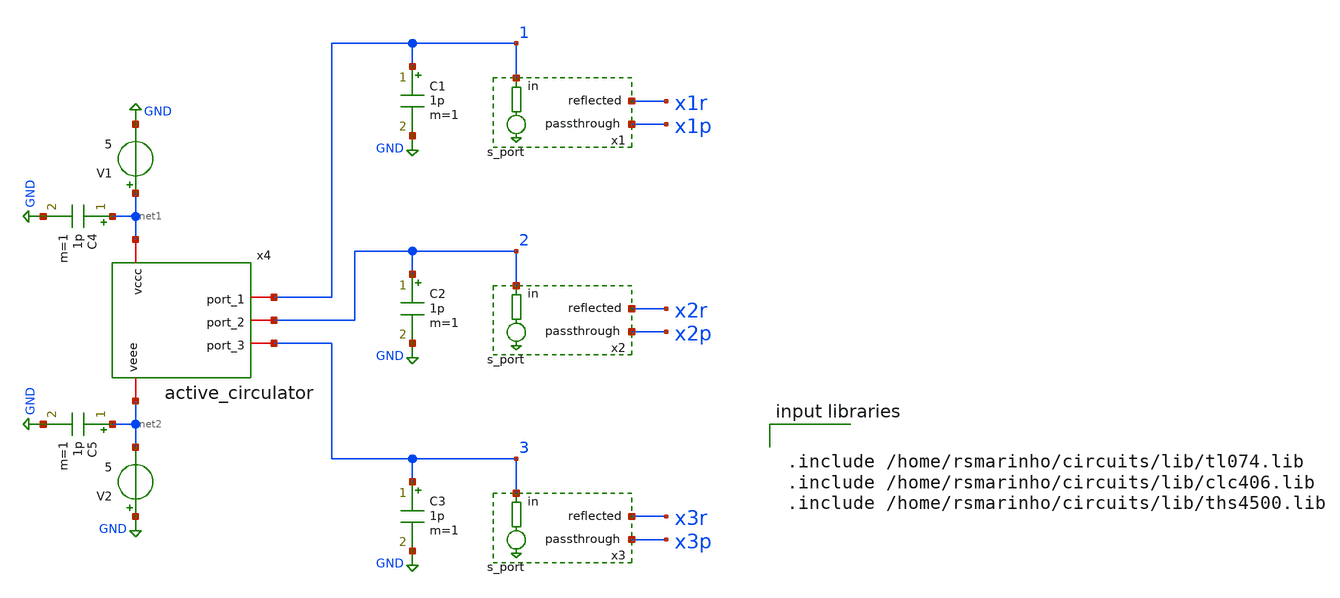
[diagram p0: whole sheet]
** sch_path: circulator/circulator_sparam.sch
**.subckt circulator_sparam
V1 net1 GND 5
V2 GND net2 5
C1 1 GND 1p m=1
C2 2 GND 1p m=1
C3 3 GND 1p m=1
C4 net1 GND 1p m=1
C5 net2 GND 1p m=1
x1 1 x1p x1r s_port Rbase=50 RS1=1e-6 RS2=1e12
x2 2 x2p x2r s_port Rbase=50 RS1=1e-6 RS2=1e12
x3 3 x3p x3r s_port Rbase=50 RS1=1e-6 RS2=1e12
x4 1 net1 2 3 net2 active_circulator
**** begin user architecture code



.options method=gear
.options savecurrents
.save all

** Check the two ac lines below for being equal!
.control
set noaskquit
set filetype=ascii

alter @c1[c] = 10p
alter @c2[c] = 10p
alter @c3[c] = 10p

** set input and output

alter R.x1.R1 = 1e-6
alter R.x1.R2 = 1e12

alter R.x2.R1 = 1e12
alter R.x2.R2 = 1e-6
alter R.x3.R1 = 1e12
alter R.x3.R2 = 1e-6

*** measurement for s11 and s21
op
** first ac measurement (change this line only together with following ac line)
ac lin 1000 1Meg 2G

**

** switch input and output

alter R.x2.R1 = 1e-6
alter R.x2.R2 = 1e12

alter R.x1.R1 = 1e12
alter R.x1.R2 = 1e-6
alter R.x3.R1 = 1e12
alter R.x3.R2 = 1e-6

*** measurement for s12 and s22
op
** second ac measurement (change this line only together with ac line above)
ac lin 1000 1Meg 2G

**

** switch input and output

alter R.x3.R1 = 1e-6
alter R.x3.R2 = 1e12

alter R.x1.R1 = 1e12
alter R.x1.R2 = 1e-6
alter R.x2.R1 = 1e12
alter R.x2.R2 = 1e-6

*** measurement for s12 and s22
op
** second ac measurement (change this line only together with ac line above)
ac lin 1000 1Meg 2G

**

** set s-param
let s11 = ac1.x1r
let s21 = ac1.x2p
let s31 = ac1.x3p

let s12 = ac2.x1p
let s22 = ac2.x2r
let s32 = ac2.x3p

let s13 = ac3.x1p
let s23 = ac3.x2p
let s33 = ac3.x3r

settype s-param s11 s21 s31 s12 s22 s32 s13 s23 s33


** set s-param db
let s11db = db(s11)
let s21db = db(s21)
let s31db = db(s31)

let s12db = db(s12)
let s22db = db(s22)
let s32db = db(s32)

let s13db = db(s13)
let s23db = db(s23)
let s33db = db(s33)

settype decibel s11db s21db s31db s12db s22db s32db s13db s23db s33db

** plot

plot xlog s11db s21db s31db
plot xlog s12db s22db s32db
plot xlog s13db s23db s33db

* gain
*plot xlog s12db s23db s31db

* isolation
*plot xlog s21db s32db s13db

* reflection
*plot xlog s11db s22db s33db

.endc
.end



.include /home/rsmarinho/circuits/lib/tl074.lib
.include /home/rsmarinho/circuits/lib/clc406.lib
.include /home/rsmarinho/circuits/lib/ths4500.lib

**** end user architecture code
**.ends

* expanding   symbol:  sparam/s_port.sym # of pins=3
** sym_path: sparam/s_port.sym
** sch_path: sparam/s_port.sch
.subckt s_port in passthrough reflected  Rbase=50 RS1=1e-6 RS2=1e12
*.iopin in
*.opin reflected
*.opin passthrough
Rout s2 8 Rbase m=1
Vdc 8 GND DC {Vbias_out} AC 0
E2 passthrough GND s2 GND 2
Vacdc 1 GND DC {Vbias_in} AC 1
Rin 1 s1 Rbase m=1
E1 3 GND s1 GND 2
Vac 3 4 DC 0 AC 1
Rloop reflected 4 1e-6 m=1
R3 reflected GND 1 m=1
.param Vbias_in = 0
R1 in s1 {RS1} m=1
R2 in s2 {RS2} m=1
.param Vbias_out = 0
.ends


* expanding   symbol:  circulator/active_circulator.sym # of pins=5
** sym_path: circulator/active_circulator.sym
** sch_path: circulator/active_circulator.sch
.subckt active_circulator port_1 vccc port_2 port_3 veee
*.iopin port_1
*.iopin port_2
*.iopin port_3
*.iopin vccc
*.iopin veee
R1 port_1 net3 100 m=1
R2 net2 net1 323.6 m=1
R3 net1 GND 100 m=1
R4 net3 net4 323.6 m=1
R5 net2 port_1 100 m=1
R6 port_2 net6 150 m=1
R7 net4 net5 485.4 m=1
R8 net5 GND 150 m=1
R9 net6 net7 485.4 m=1
R10 net4 port_2 150 m=1
R11 port_3 net9 100 m=1
R12 net7 net8 323.6 m=1
R13 net8 GND 100 m=1
R14 net9 net2 323.6 m=1
R15 net7 port_3 100 m=1
x1 net1 net3 net4 vccc veee clc406
x2 net5 net6 net7 vccc veee clc406
x3 net8 net9 net2 vccc veee clc406
.ends

.GLOBAL GND
.end
